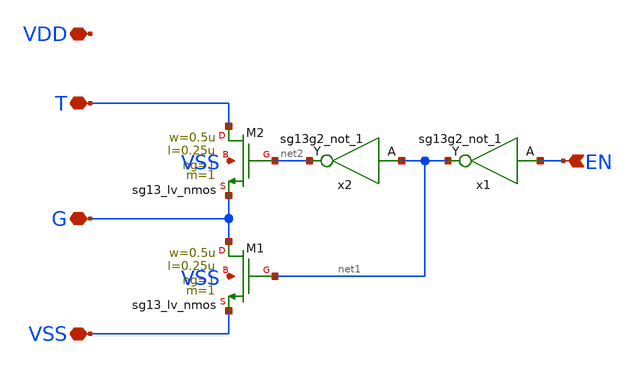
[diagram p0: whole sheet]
** sch_path: ip/riosc/xschem/trimsw.sch
**.subckt trimsw G VSS T EN VDD
*.iopin G
*.iopin VSS
*.iopin T
*.ipin EN
*.iopin VDD
XM1 G net1 VSS VSS sg13_lv_nmos w=0.5u l=0.25u ng=1 m=1 mm_ok=1
XM2 T net2 G VSS sg13_lv_nmos w=0.5u l=0.25u ng=1 m=1 mm_ok=1
x1 net1 EN VDD VSS sg13g2_not_1
x2 net2 net1 VDD VSS sg13g2_not_1
**.ends
.end
